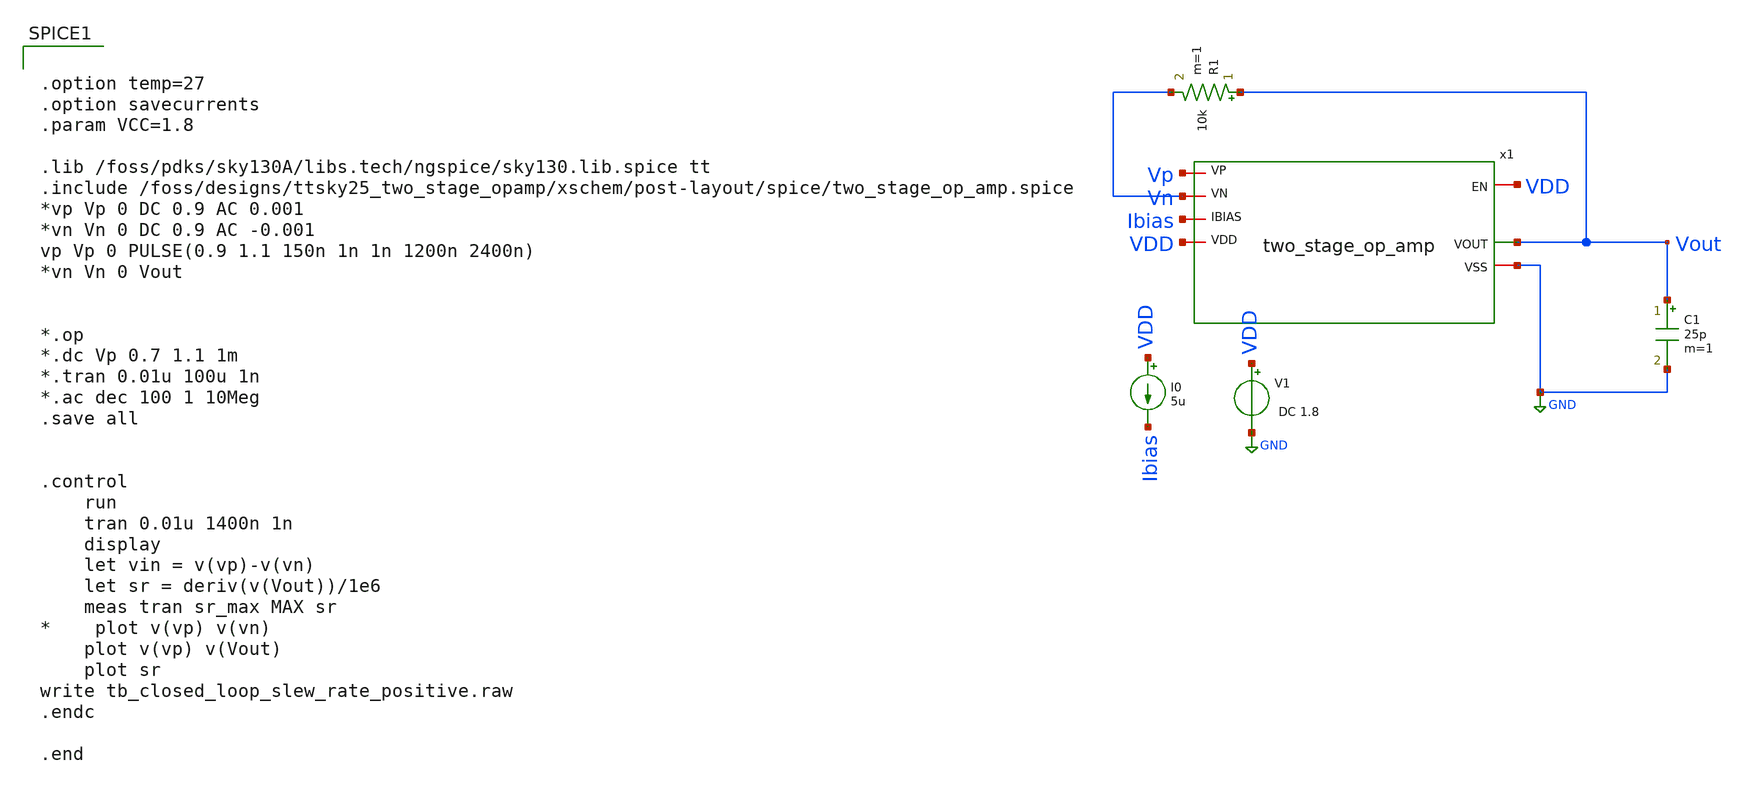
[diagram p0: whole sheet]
** sch_path: xschem/post-layout/testbenches/tb_closed_loop_slew_rate_positive.sch
**.subckt tb_closed_loop_slew_rate_positive
V1 VDD GND DC 1.8
I0 VDD Ibias 5u
C1 Vout GND 25p m=1
R1 Vout Vn 10k m=1
x1 VDD GND Ibias Vout Vp Vn VDD two_stage_op_amp
**** begin user architecture code


.option temp=27
.option savecurrents
.param VCC=1.8

.lib /foss/pdks/sky130A/libs.tech/ngspice/sky130.lib.spice tt
.include /foss/designs/ttsky25_two_stage_opamp/xschem/post-layout/spice/two_stage_op_amp.spice
*vp Vp 0 DC 0.9 AC 0.001
*vn Vn 0 DC 0.9 AC -0.001
vp Vp 0 PULSE(0.9 1.1 150n 1n 1n 1200n 2400n)
*vn Vn 0 Vout


*.op
*.dc Vp 0.7 1.1 1m
*.tran 0.01u 100u 1n
*.ac dec 100 1 10Meg
.save all


.control
	run
	tran 0.01u 1400n 1n
	display
	let vin = v(vp)-v(vn)
	let sr = deriv(v(Vout))/1e6
	meas tran sr_max MAX sr
*	plot v(vp) v(vn)
	plot v(vp) v(Vout)
	plot sr
write tb_closed_loop_slew_rate_positive.raw
.endc

.end


**** end user architecture code
**.ends
.GLOBAL GND
.end
